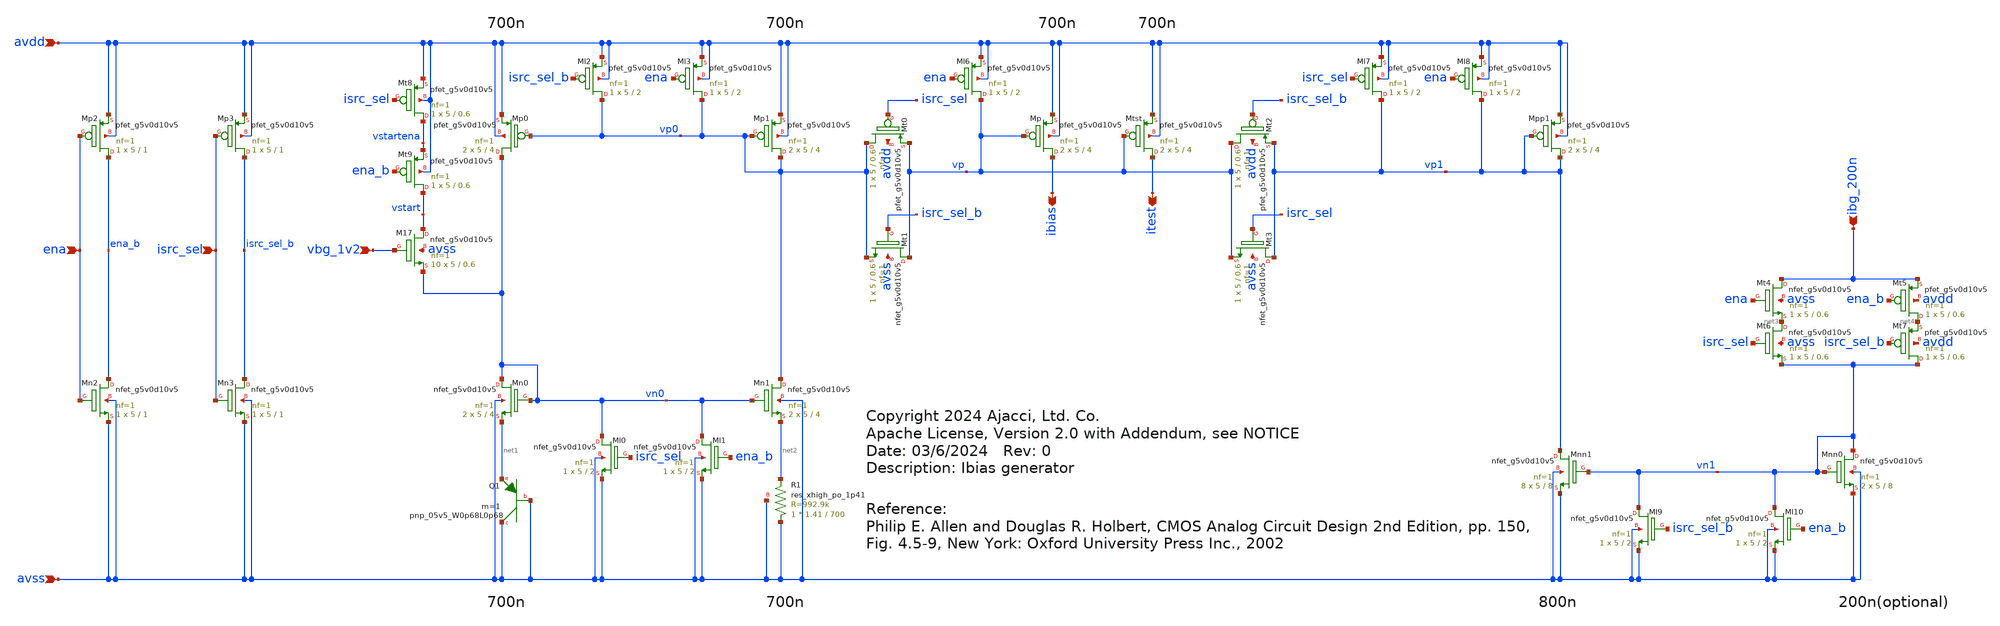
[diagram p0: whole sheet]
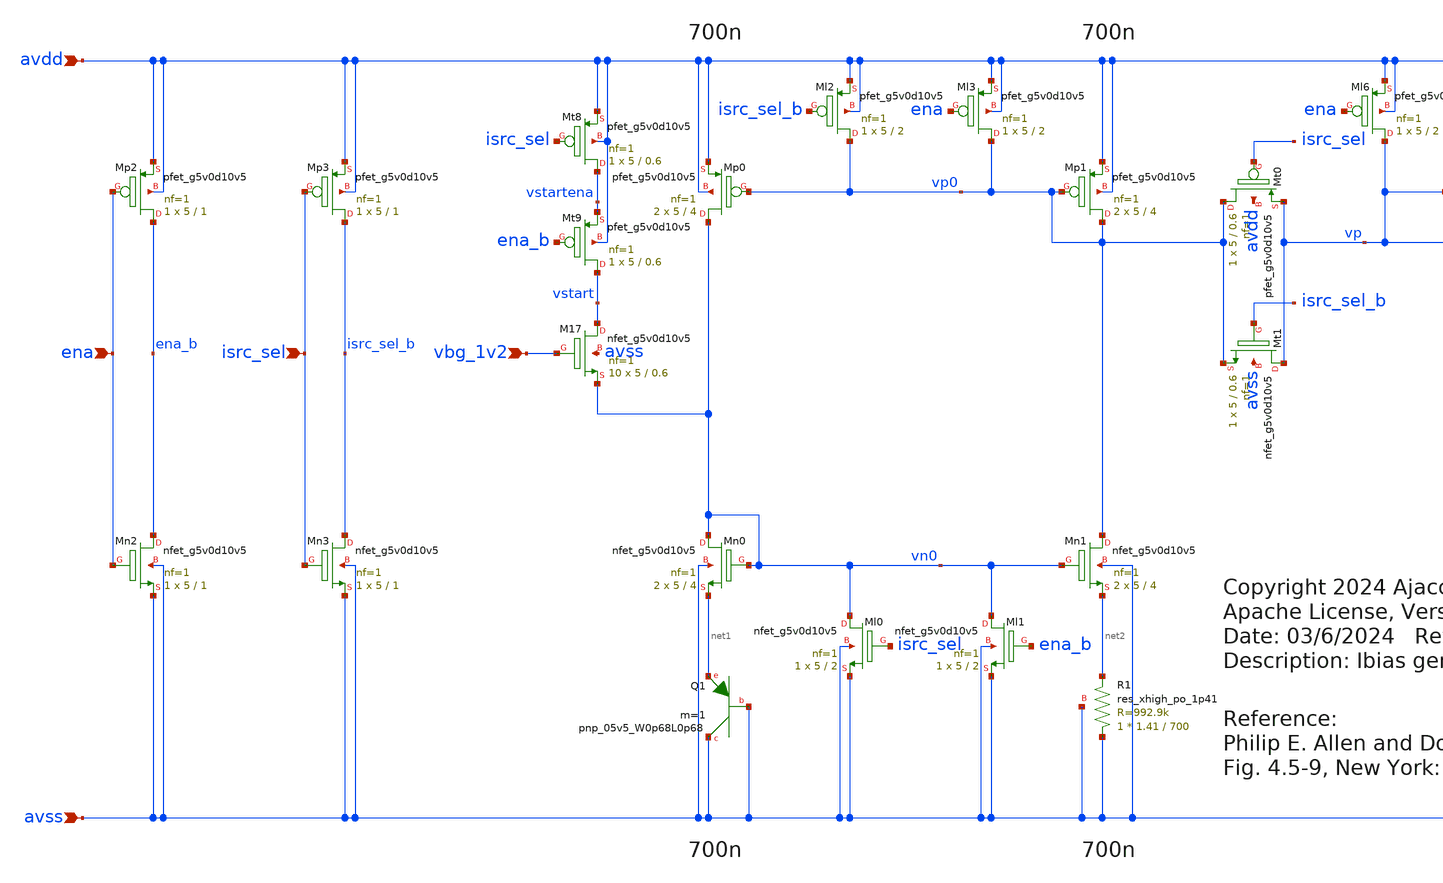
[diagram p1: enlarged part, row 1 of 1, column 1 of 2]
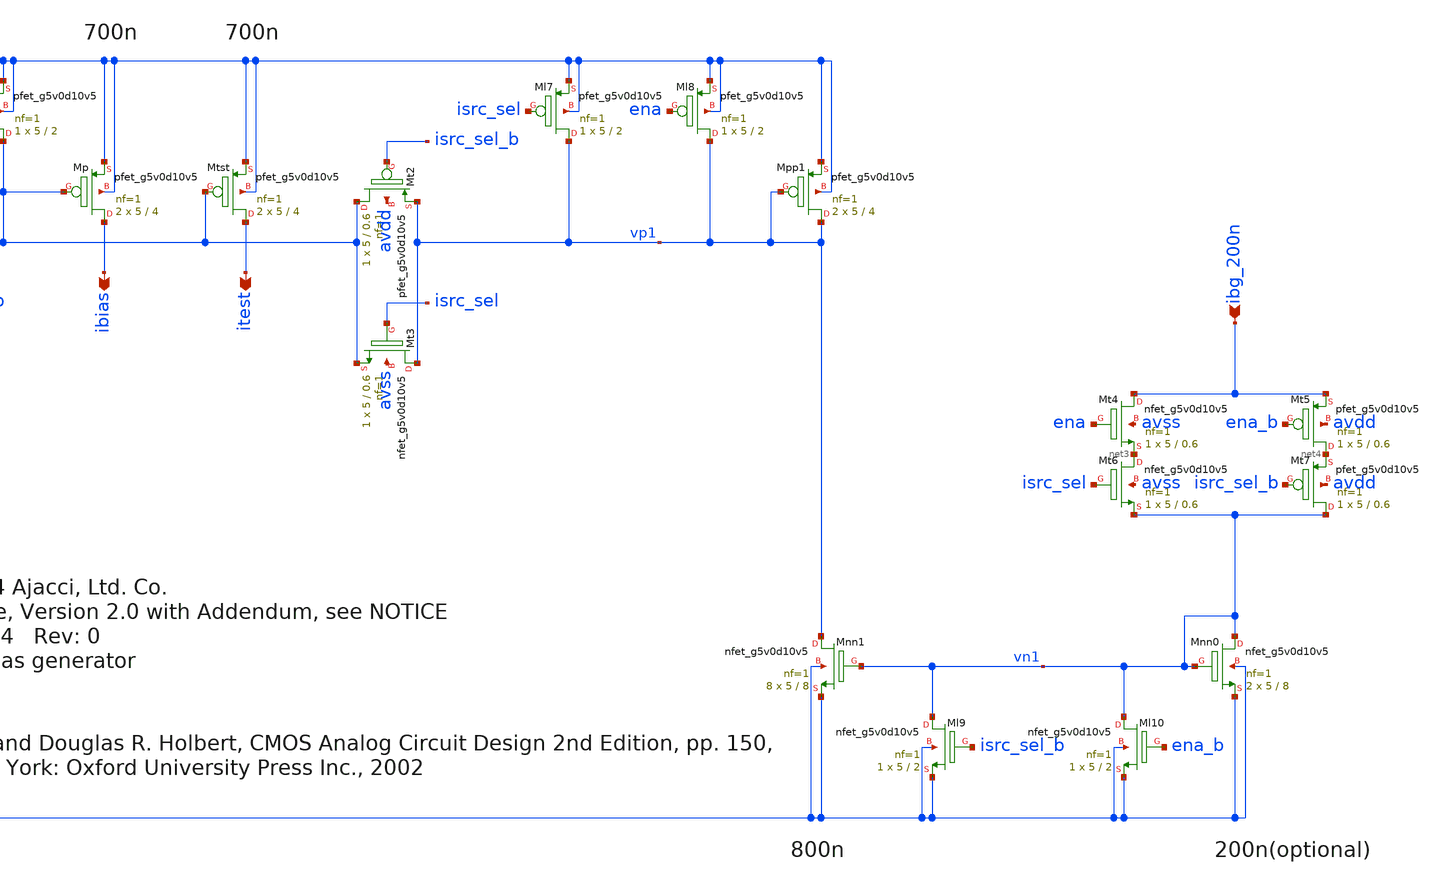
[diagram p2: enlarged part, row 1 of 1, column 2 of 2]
** sch_path: xschem/ibias_gen.sch
* Copyright 2024 Ajacci, Ltd. Co.
* Apache License, Version 2.0 with Addendum, see NOTICE
**.subckt ibias_gen vbg_1v2 ena ibias ibg_200n isrc_sel avdd avss itest
*.ipin vbg_1v2
*.ipin ena
*.opin ibias
*.ipin ibg_200n
*.ipin isrc_sel
*.ipin avdd
*.ipin avss
*.opin itest
XQ1 avss avss net1 sky130_fd_pr__pnp_05v5_W0p68L0p68 m=1
XM17 vstart vbg_1v2 vn0 avss sky130_fd_pr__nfet_g5v0d10v5 L=0.6 W=5 nf=1 ad='int((nf+1)/2) * W/nf * 0.29'
+ as='int((nf+2)/2) * W/nf * 0.29' pd='2*int((nf+1)/2) * (W/nf + 0.29)' ps='2*int((nf+2)/2) * (W/nf + 0.29)'
+ nrd='0.29 / W' nrs='0.29 / W' sa=0 sb=0 sd=0 mult=10 m=10
XMt9 vstart ena_b vstartena avdd sky130_fd_pr__pfet_g5v0d10v5 L=0.6 W=5 nf=1 ad='int((nf+1)/2) * W/nf * 0.29'
+ as='int((nf+2)/2) * W/nf * 0.29' pd='2*int((nf+1)/2) * (W/nf + 0.29)' ps='2*int((nf+2)/2) * (W/nf + 0.29)'
+ nrd='0.29 / W' nrs='0.29 / W' sa=0 sb=0 sd=0 mult=1 m=1
XMn0 vn0 vn0 net1 avss sky130_fd_pr__nfet_g5v0d10v5 L=4 W=5 nf=1 ad='int((nf+1)/2) * W/nf * 0.29' as='int((nf+2)/2) * W/nf * 0.29'
+ pd='2*int((nf+1)/2) * (W/nf + 0.29)' ps='2*int((nf+2)/2) * (W/nf + 0.29)' nrd='0.29 / W' nrs='0.29 / W'
+ sa=0 sb=0 sd=0 mult=2 m=2
XMp0 vn0 vp0 avdd avdd sky130_fd_pr__pfet_g5v0d10v5 L=4 W=5 nf=1 ad='int((nf+1)/2) * W/nf * 0.29' as='int((nf+2)/2) * W/nf * 0.29'
+ pd='2*int((nf+1)/2) * (W/nf + 0.29)' ps='2*int((nf+2)/2) * (W/nf + 0.29)' nrd='0.29 / W' nrs='0.29 / W'
+ sa=0 sb=0 sd=0 mult=2 m=2
XMn1 vp0 vn0 net2 avss sky130_fd_pr__nfet_g5v0d10v5 L=4 W=5 nf=1 ad='int((nf+1)/2) * W/nf * 0.29' as='int((nf+2)/2) * W/nf * 0.29'
+ pd='2*int((nf+1)/2) * (W/nf + 0.29)' ps='2*int((nf+2)/2) * (W/nf + 0.29)' nrd='0.29 / W' nrs='0.29 / W'
+ sa=0 sb=0 sd=0 mult=2 m=2
XMp1 vp0 vp0 avdd avdd sky130_fd_pr__pfet_g5v0d10v5 L=4 W=5 nf=1 ad='int((nf+1)/2) * W/nf * 0.29' as='int((nf+2)/2) * W/nf * 0.29'
+ pd='2*int((nf+1)/2) * (W/nf + 0.29)' ps='2*int((nf+2)/2) * (W/nf + 0.29)' nrd='0.29 / W' nrs='0.29 / W'
+ sa=0 sb=0 sd=0 mult=2 m=2
XMp ibias vp avdd avdd sky130_fd_pr__pfet_g5v0d10v5 L=4 W=5 nf=1 ad='int((nf+1)/2) * W/nf * 0.29' as='int((nf+2)/2) * W/nf * 0.29'
+ pd='2*int((nf+1)/2) * (W/nf + 0.29)' ps='2*int((nf+2)/2) * (W/nf + 0.29)' nrd='0.29 / W' nrs='0.29 / W'
+ sa=0 sb=0 sd=0 mult=2 m=2
XMt0 vp0 isrc_sel vp avdd sky130_fd_pr__pfet_g5v0d10v5 L=0.6 W=5 nf=1 ad='int((nf+1)/2) * W/nf * 0.29'
+ as='int((nf+2)/2) * W/nf * 0.29' pd='2*int((nf+1)/2) * (W/nf + 0.29)' ps='2*int((nf+2)/2) * (W/nf + 0.29)'
+ nrd='0.29 / W' nrs='0.29 / W' sa=0 sb=0 sd=0 mult=1 m=1
XMt1 vp isrc_sel_b vp0 avss sky130_fd_pr__nfet_g5v0d10v5 L=0.6 W=5 nf=1 ad='int((nf+1)/2) * W/nf * 0.29'
+ as='int((nf+2)/2) * W/nf * 0.29' pd='2*int((nf+1)/2) * (W/nf + 0.29)' ps='2*int((nf+2)/2) * (W/nf + 0.29)'
+ nrd='0.29 / W' nrs='0.29 / W' sa=0 sb=0 sd=0 mult=1 m=1
XMl6 vp ena avdd avdd sky130_fd_pr__pfet_g5v0d10v5 L=2 W=5 nf=1 ad='int((nf+1)/2) * W/nf * 0.29' as='int((nf+2)/2) * W/nf * 0.29'
+ pd='2*int((nf+1)/2) * (W/nf + 0.29)' ps='2*int((nf+2)/2) * (W/nf + 0.29)' nrd='0.29 / W' nrs='0.29 / W'
+ sa=0 sb=0 sd=0 mult=1 m=1
XMl3 vp0 ena avdd avdd sky130_fd_pr__pfet_g5v0d10v5 L=2 W=5 nf=1 ad='int((nf+1)/2) * W/nf * 0.29' as='int((nf+2)/2) * W/nf * 0.29'
+ pd='2*int((nf+1)/2) * (W/nf + 0.29)' ps='2*int((nf+2)/2) * (W/nf + 0.29)' nrd='0.29 / W' nrs='0.29 / W'
+ sa=0 sb=0 sd=0 mult=1 m=1
XMl1 vn0 ena_b avss avss sky130_fd_pr__nfet_g5v0d10v5 L=2 W=5 nf=1 ad='int((nf+1)/2) * W/nf * 0.29' as='int((nf+2)/2) * W/nf * 0.29'
+ pd='2*int((nf+1)/2) * (W/nf + 0.29)' ps='2*int((nf+2)/2) * (W/nf + 0.29)' nrd='0.29 / W' nrs='0.29 / W'
+ sa=0 sb=0 sd=0 mult=1 m=1
XMnn1 vp1 vn1 avss avss sky130_fd_pr__nfet_g5v0d10v5 L=8 W=5 nf=1 ad='int((nf+1)/2) * W/nf * 0.29' as='int((nf+2)/2) * W/nf * 0.29'
+ pd='2*int((nf+1)/2) * (W/nf + 0.29)' ps='2*int((nf+2)/2) * (W/nf + 0.29)' nrd='0.29 / W' nrs='0.29 / W'
+ sa=0 sb=0 sd=0 mult=8 m=8
XMnn0 vn1 vn1 avss avss sky130_fd_pr__nfet_g5v0d10v5 L=8 W=5 nf=1 ad='int((nf+1)/2) * W/nf * 0.29' as='int((nf+2)/2) * W/nf * 0.29'
+ pd='2*int((nf+1)/2) * (W/nf + 0.29)' ps='2*int((nf+2)/2) * (W/nf + 0.29)' nrd='0.29 / W' nrs='0.29 / W'
+ sa=0 sb=0 sd=0 mult=2 m=2
XMl9 vn1 isrc_sel_b avss avss sky130_fd_pr__nfet_g5v0d10v5 L=2 W=5 nf=1 ad='int((nf+1)/2) * W/nf * 0.29'
+ as='int((nf+2)/2) * W/nf * 0.29' pd='2*int((nf+1)/2) * (W/nf + 0.29)' ps='2*int((nf+2)/2) * (W/nf + 0.29)'
+ nrd='0.29 / W' nrs='0.29 / W' sa=0 sb=0 sd=0 mult=1 m=1
XMt6 net3 isrc_sel vn1 avss sky130_fd_pr__nfet_g5v0d10v5 L=0.6 W=5 nf=1 ad='int((nf+1)/2) * W/nf * 0.29'
+ as='int((nf+2)/2) * W/nf * 0.29' pd='2*int((nf+1)/2) * (W/nf + 0.29)' ps='2*int((nf+2)/2) * (W/nf + 0.29)'
+ nrd='0.29 / W' nrs='0.29 / W' sa=0 sb=0 sd=0 mult=1 m=1
XMt7 vn1 isrc_sel_b net4 avdd sky130_fd_pr__pfet_g5v0d10v5 L=0.6 W=5 nf=1 ad='int((nf+1)/2) * W/nf * 0.29'
+ as='int((nf+2)/2) * W/nf * 0.29' pd='2*int((nf+1)/2) * (W/nf + 0.29)' ps='2*int((nf+2)/2) * (W/nf + 0.29)'
+ nrd='0.29 / W' nrs='0.29 / W' sa=0 sb=0 sd=0 mult=1 m=1
XMpp1 vp1 vp1 avdd avdd sky130_fd_pr__pfet_g5v0d10v5 L=4 W=5 nf=1 ad='int((nf+1)/2) * W/nf * 0.29' as='int((nf+2)/2) * W/nf * 0.29'
+ pd='2*int((nf+1)/2) * (W/nf + 0.29)' ps='2*int((nf+2)/2) * (W/nf + 0.29)' nrd='0.29 / W' nrs='0.29 / W'
+ sa=0 sb=0 sd=0 mult=2 m=2
XMt2 vp isrc_sel_b vp1 avdd sky130_fd_pr__pfet_g5v0d10v5 L=0.6 W=5 nf=1 ad='int((nf+1)/2) * W/nf * 0.29'
+ as='int((nf+2)/2) * W/nf * 0.29' pd='2*int((nf+1)/2) * (W/nf + 0.29)' ps='2*int((nf+2)/2) * (W/nf + 0.29)'
+ nrd='0.29 / W' nrs='0.29 / W' sa=0 sb=0 sd=0 mult=1 m=1
XMt3 vp1 isrc_sel vp avss sky130_fd_pr__nfet_g5v0d10v5 L=0.6 W=5 nf=1 ad='int((nf+1)/2) * W/nf * 0.29'
+ as='int((nf+2)/2) * W/nf * 0.29' pd='2*int((nf+1)/2) * (W/nf + 0.29)' ps='2*int((nf+2)/2) * (W/nf + 0.29)'
+ nrd='0.29 / W' nrs='0.29 / W' sa=0 sb=0 sd=0 mult=1 m=1
XMt4 ibg_200n ena net3 avss sky130_fd_pr__nfet_g5v0d10v5 L=0.6 W=5 nf=1 ad='int((nf+1)/2) * W/nf * 0.29'
+ as='int((nf+2)/2) * W/nf * 0.29' pd='2*int((nf+1)/2) * (W/nf + 0.29)' ps='2*int((nf+2)/2) * (W/nf + 0.29)'
+ nrd='0.29 / W' nrs='0.29 / W' sa=0 sb=0 sd=0 mult=1 m=1
XMt5 net4 ena_b ibg_200n avdd sky130_fd_pr__pfet_g5v0d10v5 L=0.6 W=5 nf=1 ad='int((nf+1)/2) * W/nf * 0.29'
+ as='int((nf+2)/2) * W/nf * 0.29' pd='2*int((nf+1)/2) * (W/nf + 0.29)' ps='2*int((nf+2)/2) * (W/nf + 0.29)'
+ nrd='0.29 / W' nrs='0.29 / W' sa=0 sb=0 sd=0 mult=1 m=1
XMl7 vp1 isrc_sel avdd avdd sky130_fd_pr__pfet_g5v0d10v5 L=2 W=5 nf=1 ad='int((nf+1)/2) * W/nf * 0.29'
+ as='int((nf+2)/2) * W/nf * 0.29' pd='2*int((nf+1)/2) * (W/nf + 0.29)' ps='2*int((nf+2)/2) * (W/nf + 0.29)'
+ nrd='0.29 / W' nrs='0.29 / W' sa=0 sb=0 sd=0 mult=1 m=1
XMl8 vp1 ena avdd avdd sky130_fd_pr__pfet_g5v0d10v5 L=2 W=5 nf=1 ad='int((nf+1)/2) * W/nf * 0.29' as='int((nf+2)/2) * W/nf * 0.29'
+ pd='2*int((nf+1)/2) * (W/nf + 0.29)' ps='2*int((nf+2)/2) * (W/nf + 0.29)' nrd='0.29 / W' nrs='0.29 / W'
+ sa=0 sb=0 sd=0 mult=1 m=1
XMl10 vn1 ena_b avss avss sky130_fd_pr__nfet_g5v0d10v5 L=2 W=5 nf=1 ad='int((nf+1)/2) * W/nf * 0.29'
+ as='int((nf+2)/2) * W/nf * 0.29' pd='2*int((nf+1)/2) * (W/nf + 0.29)' ps='2*int((nf+2)/2) * (W/nf + 0.29)'
+ nrd='0.29 / W' nrs='0.29 / W' sa=0 sb=0 sd=0 mult=1 m=1
XMl2 vp0 isrc_sel_b avdd avdd sky130_fd_pr__pfet_g5v0d10v5 L=2 W=5 nf=1 ad='int((nf+1)/2) * W/nf * 0.29'
+ as='int((nf+2)/2) * W/nf * 0.29' pd='2*int((nf+1)/2) * (W/nf + 0.29)' ps='2*int((nf+2)/2) * (W/nf + 0.29)'
+ nrd='0.29 / W' nrs='0.29 / W' sa=0 sb=0 sd=0 mult=1 m=1
XMl0 vn0 isrc_sel avss avss sky130_fd_pr__nfet_g5v0d10v5 L=2 W=5 nf=1 ad='int((nf+1)/2) * W/nf * 0.29'
+ as='int((nf+2)/2) * W/nf * 0.29' pd='2*int((nf+1)/2) * (W/nf + 0.29)' ps='2*int((nf+2)/2) * (W/nf + 0.29)'
+ nrd='0.29 / W' nrs='0.29 / W' sa=0 sb=0 sd=0 mult=1 m=1
XMt8 vstartena isrc_sel avdd avdd sky130_fd_pr__pfet_g5v0d10v5 L=0.6 W=5 nf=1 ad='int((nf+1)/2) * W/nf * 0.29'
+ as='int((nf+2)/2) * W/nf * 0.29' pd='2*int((nf+1)/2) * (W/nf + 0.29)' ps='2*int((nf+2)/2) * (W/nf + 0.29)'
+ nrd='0.29 / W' nrs='0.29 / W' sa=0 sb=0 sd=0 mult=1 m=1
XMn2 ena_b ena avss avss sky130_fd_pr__nfet_g5v0d10v5 L=1 W=5 nf=1 ad='int((nf+1)/2) * W/nf * 0.29' as='int((nf+2)/2) * W/nf * 0.29'
+ pd='2*int((nf+1)/2) * (W/nf + 0.29)' ps='2*int((nf+2)/2) * (W/nf + 0.29)' nrd='0.29 / W' nrs='0.29 / W'
+ sa=0 sb=0 sd=0 mult=1 m=1
XMp2 ena_b ena avdd avdd sky130_fd_pr__pfet_g5v0d10v5 L=1 W=5 nf=1 ad='int((nf+1)/2) * W/nf * 0.29' as='int((nf+2)/2) * W/nf * 0.29'
+ pd='2*int((nf+1)/2) * (W/nf + 0.29)' ps='2*int((nf+2)/2) * (W/nf + 0.29)' nrd='0.29 / W' nrs='0.29 / W'
+ sa=0 sb=0 sd=0 mult=1 m=1
XMn3 isrc_sel_b isrc_sel avss avss sky130_fd_pr__nfet_g5v0d10v5 L=1 W=5 nf=1 ad='int((nf+1)/2) * W/nf * 0.29'
+ as='int((nf+2)/2) * W/nf * 0.29' pd='2*int((nf+1)/2) * (W/nf + 0.29)' ps='2*int((nf+2)/2) * (W/nf + 0.29)'
+ nrd='0.29 / W' nrs='0.29 / W' sa=0 sb=0 sd=0 mult=1 m=1
XMp3 isrc_sel_b isrc_sel avdd avdd sky130_fd_pr__pfet_g5v0d10v5 L=1 W=5 nf=1 ad='int((nf+1)/2) * W/nf * 0.29'
+ as='int((nf+2)/2) * W/nf * 0.29' pd='2*int((nf+1)/2) * (W/nf + 0.29)' ps='2*int((nf+2)/2) * (W/nf + 0.29)'
+ nrd='0.29 / W' nrs='0.29 / W' sa=0 sb=0 sd=0 mult=1 m=1
XMtst itest vp avdd avdd sky130_fd_pr__pfet_g5v0d10v5 L=4 W=5 nf=1 ad='int((nf+1)/2) * W/nf * 0.29' as='int((nf+2)/2) * W/nf * 0.29'
+ pd='2*int((nf+1)/2) * (W/nf + 0.29)' ps='2*int((nf+2)/2) * (W/nf + 0.29)' nrd='0.29 / W' nrs='0.29 / W'
+ sa=0 sb=0 sd=0 mult=2 m=2
XR1 avss net2 avss sky130_fd_pr__res_xhigh_po_1p41 L=700 mult=1 m=1
**.ends
.end
